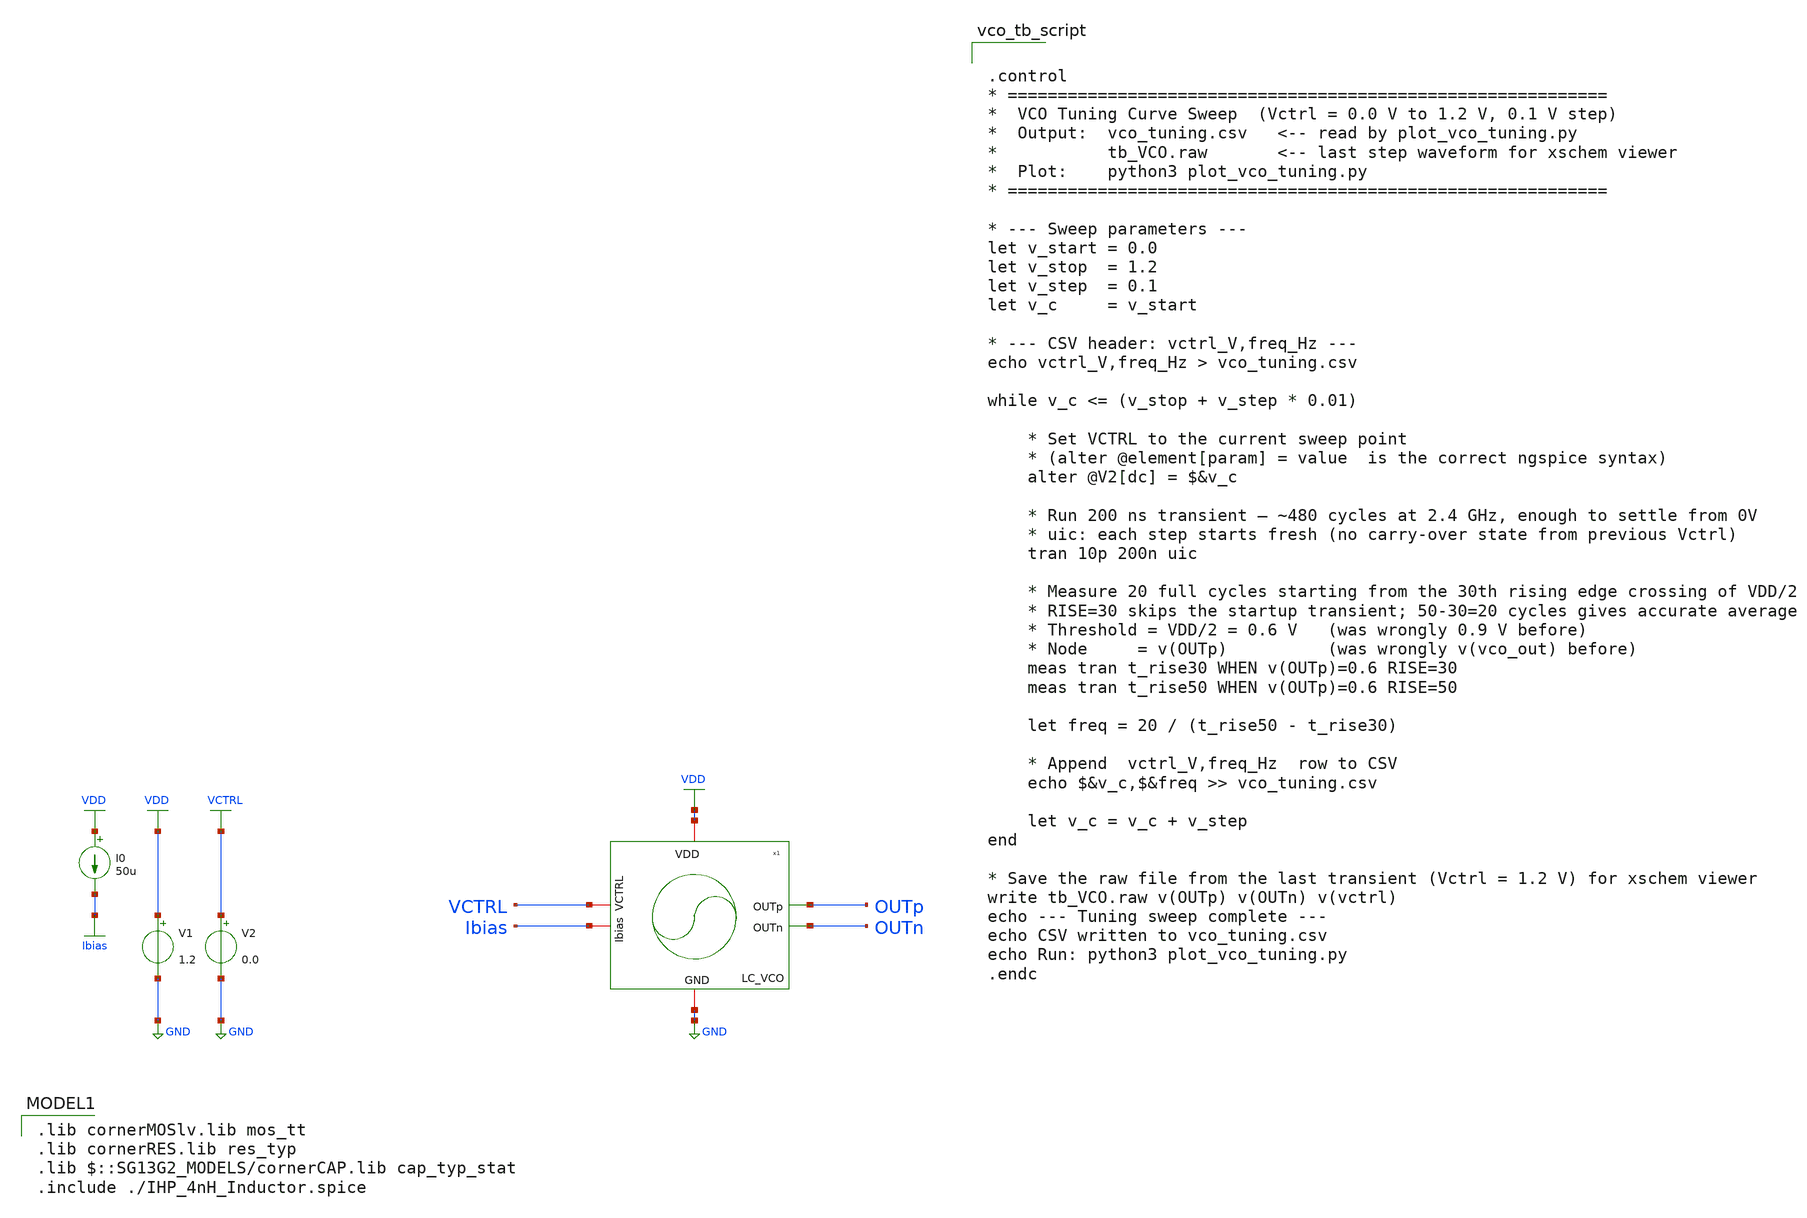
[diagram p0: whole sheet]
** sch_path: schematic/top-pll/lc-vco/LC_VCO_response_tb.sch
**.subckt LC_VCO_response_tb
V2 VCTRL GND 0.0
x2 VDD OUTp OUTn Ibias VCTRL GND LC_VCO
V1 VDD GND 1.2
I0 VDD Ibias 50u
**** begin user architecture code


.control
* ============================================================
*  VCO Tuning Curve Sweep  (Vctrl = 0.0 V to 1.2 V, 0.1 V step)
*  Output:  vco_tuning.csv   <-- read by plot_vco_tuning.py
*           tb_VCO.raw       <-- last step waveform for xschem viewer
*  Plot:    python3 plot_vco_tuning.py
* ============================================================

* --- Sweep parameters ---
let v_start = 0.0
let v_stop  = 1.2
let v_step  = 0.1
let v_c     = v_start

* --- CSV header: vctrl_V,freq_Hz ---
echo vctrl_V,freq_Hz > vco_tuning.csv

while v_c <= (v_stop + v_step * 0.01)

    * Set VCTRL to the current sweep point
    * (alter @element[param] = value  is the correct ngspice syntax)
    alter @V2[dc] = $&v_c

    * Run 200 ns transient — ~480 cycles at 2.4 GHz, enough to settle from 0V
    * uic: each step starts fresh (no carry-over state from previous Vctrl)
    tran 10p 200n uic

    * Measure 20 full cycles starting from the 30th rising edge crossing of VDD/2
    * RISE=30 skips the startup transient; 50-30=20 cycles gives accurate average
    * Threshold = VDD/2 = 0.6 V   (was wrongly 0.9 V before)
    * Node     = v(OUTp)          (was wrongly v(vco_out) before)
    meas tran t_rise30 WHEN v(OUTp)=0.6 RISE=30
    meas tran t_rise50 WHEN v(OUTp)=0.6 RISE=50

    let freq = 20 / (t_rise50 - t_rise30)

    * Append  vctrl_V,freq_Hz  row to CSV
    echo $&v_c,$&freq >> vco_tuning.csv

    let v_c = v_c + v_step
end

* Save the raw file from the last transient (Vctrl = 1.2 V) for xschem viewer
write tb_VCO.raw v(OUTp) v(OUTn) v(vctrl)
echo --- Tuning sweep complete ---
echo CSV written to vco_tuning.csv
echo Run: python3 plot_vco_tuning.py
.endc


 .lib cornerMOSlv.lib mos_tt
.lib cornerRES.lib res_typ
.lib $::SG13G2_MODELS/cornerCAP.lib cap_typ_stat
.include ./IHP_4nH_Inductor.spice

**** end user architecture code
**.ends
.GLOBAL GND
.GLOBAL VCTRL
.GLOBAL VDD
.GLOBAL Ibias
.end
